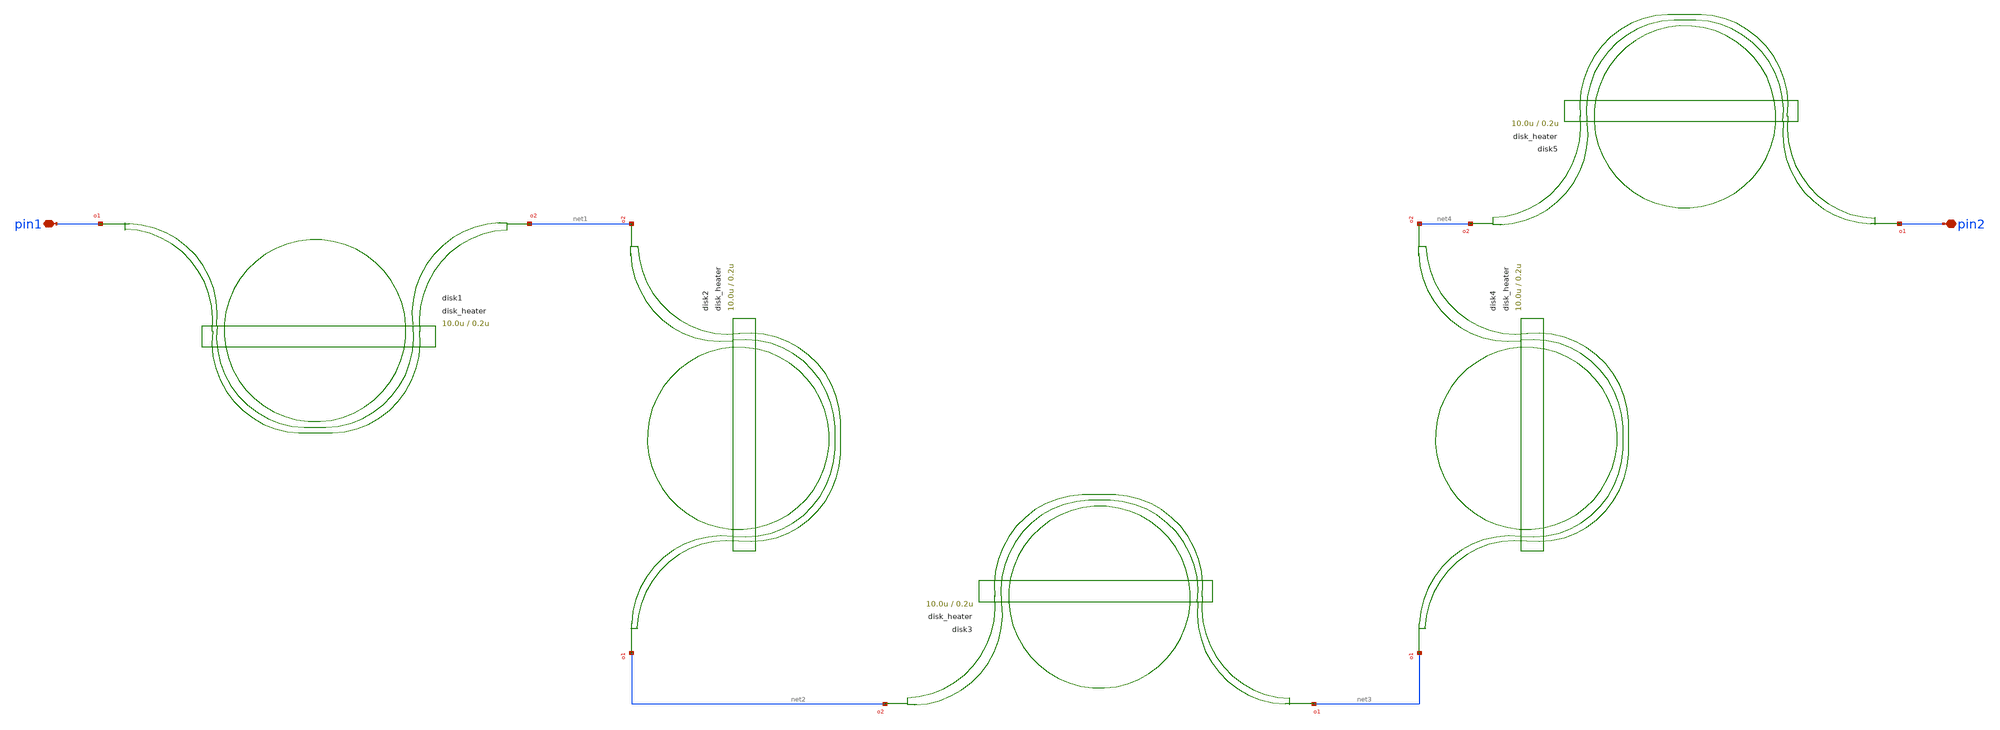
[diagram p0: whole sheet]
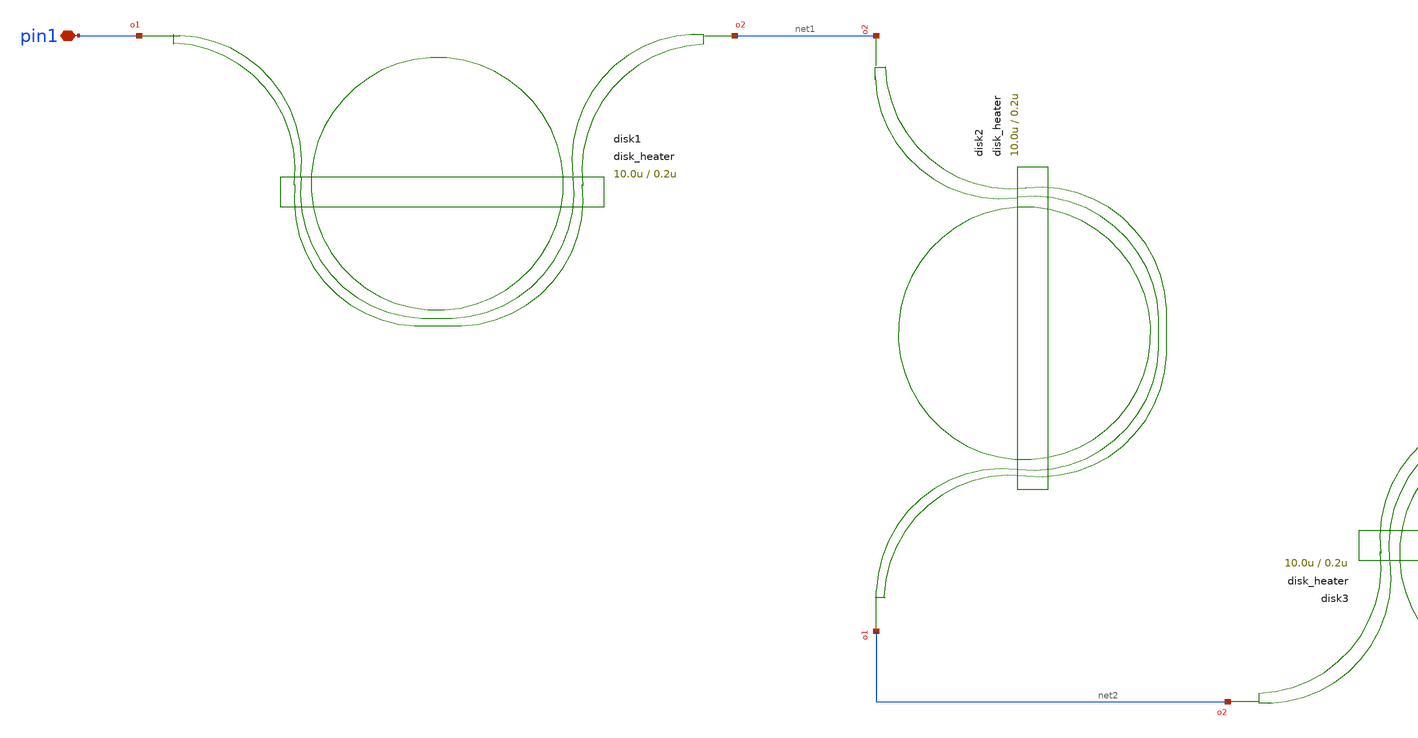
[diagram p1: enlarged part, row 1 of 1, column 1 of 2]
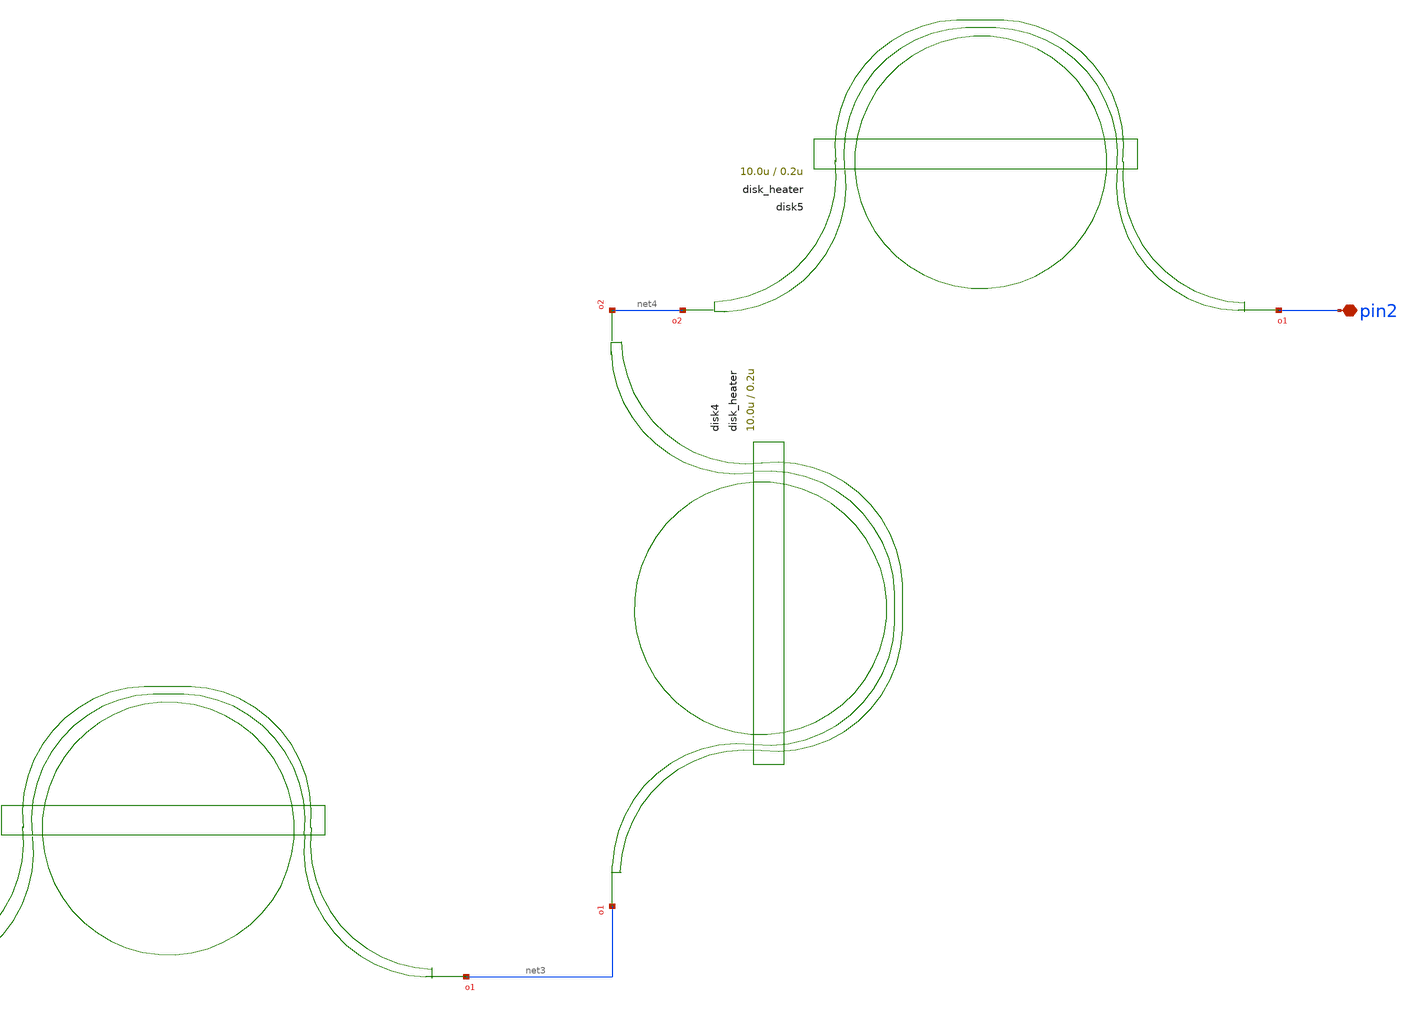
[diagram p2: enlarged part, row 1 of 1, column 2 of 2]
** sch_path: xschem/tests/test_sch/test_disk_heater.sch
* Copyright (c) 2024, Mabrains LLC
* Licensed under the GNU Lesser General Public License, Version 3.0 (the "License");
* you may not use this file except in compliance with the License.
* GNU Lesser General Public License
* Version 3, 29 June 2007
* This program is free software: you can redistribute it and/or modify
* it under the terms of the GNU Lesser General Public License as published
* by the Free Software Foundation, either version 3 of the License, or
* (at your option) any later version.
* This program is distributed in the hope that it will be useful,
* but WITHOUT ANY WARRANTY; without even the implied warranty of
* MERCHANTABILITY or FITNESS FOR A PARTICULAR PURPOSE.  See the
* GNU Lesser General Public License for more details.
* You should have received a copy of the GNU Lesser General Public License
* along with this program.  If not, see <https://www.gnu.org/licenses/>.
* SPDX-License-Identifier: LGPL-3.0
**.subckt test_disk_heater pin1 pin2
*.iopin pin1
*.iopin pin2
Pdisk1 pin1 net1 disk_heater radius=10.0u gap=0.2u wrap_angle_deg=180.0 parity=1 heater_width=5.0u
+ heater_extent=2.0u
Pdisk2 net2 net1 disk_heater radius=10.0u gap=0.2u wrap_angle_deg=180.0 parity=1 heater_width=5.0u
+ heater_extent=2.0u
Pdisk3 net3 net2 disk_heater radius=10.0u gap=0.2u wrap_angle_deg=180.0 parity=1 heater_width=5.0u
+ heater_extent=2.0u
Pdisk4 net3 net4 disk_heater radius=10.0u gap=0.2u wrap_angle_deg=180.0 parity=1 heater_width=5.0u
+ heater_extent=2.0u
Pdisk5 pin2 net4 disk_heater radius=10.0u gap=0.2u wrap_angle_deg=180.0 parity=1 heater_width=5.0u
+ heater_extent=2.0u
**.ends
.end
